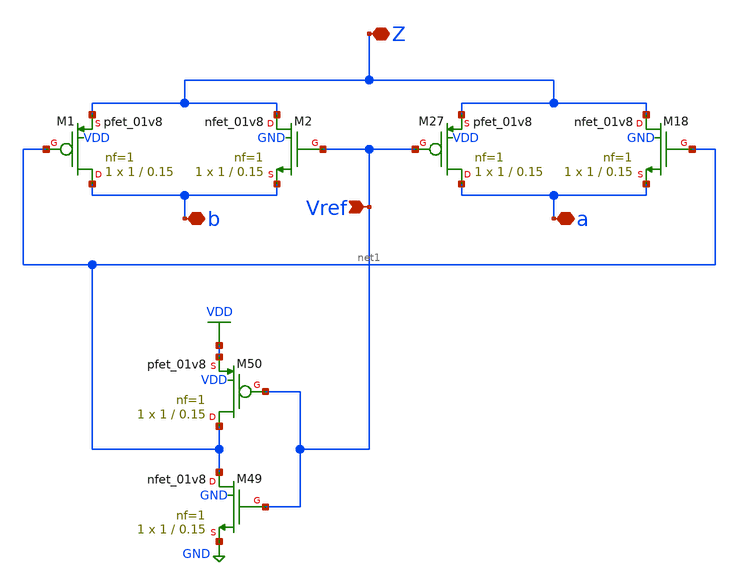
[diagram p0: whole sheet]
** sch_path: switch.sch
**.subckt switch Vref Z a b
*.ipin Vref
*.iopin Z
*.iopin a
*.iopin b
XM27 a Vref Z VDD sky130_fd_pr__pfet_01v8 L=0.15 W=1 nf=1 ad='int((1 + 1)/2) * 1 / 1 * 0.29' as='int((1 + 2)/2) * 1 / 1 * 0.29'
+ pd='2*int((1 + 1)/2) * (1 / 1 + 0.29)' ps='2*int((1 + 2)/2) * (1 / 1 + 0.29)' nrd='0.29 / 1 ' nrs='0.29 / 1 '
+ sa=0 sb=0 sd=0 mult=1 m=1
XM18 Z net1 a GND sky130_fd_pr__nfet_01v8 L=0.15 W=1 nf=1 ad='int((nf+1)/2) * W/nf * 0.29' as='int((nf+2)/2) * W/nf * 0.29'
+ pd='2*int((nf+1)/2) * (W/nf + 0.29)' ps='2*int((nf+2)/2) * (W/nf + 0.29)' nrd='0.29 / W' nrs='0.29 / W'
+ sa=0 sb=0 sd=0 mult=1 m=1
XM1 b net1 Z VDD sky130_fd_pr__pfet_01v8 L=0.15 W=1 nf=1 ad='int((1 + 1)/2) * 1 / 1 * 0.29' as='int((1 + 2)/2) * 1 / 1 * 0.29'
+ pd='2*int((1 + 1)/2) * (1 / 1 + 0.29)' ps='2*int((1 + 2)/2) * (1 / 1 + 0.29)' nrd='0.29 / 1 ' nrs='0.29 / 1 '
+ sa=0 sb=0 sd=0 mult=1 m=1
XM2 Z Vref b GND sky130_fd_pr__nfet_01v8 L=0.15 W=1 nf=1 ad='int((nf+1)/2) * W/nf * 0.29' as='int((nf+2)/2) * W/nf * 0.29'
+ pd='2*int((nf+1)/2) * (W/nf + 0.29)' ps='2*int((nf+2)/2) * (W/nf + 0.29)' nrd='0.29 / W' nrs='0.29 / W'
+ sa=0 sb=0 sd=0 mult=1 m=1
XM49 net1 Vref GND GND sky130_fd_pr__nfet_01v8 L=0.15 W=1 nf=1 ad='int((nf+1)/2) * W/nf * 0.29' as='int((nf+2)/2) * W/nf * 0.29'
+ pd='2*int((nf+1)/2) * (W/nf + 0.29)' ps='2*int((nf+2)/2) * (W/nf + 0.29)' nrd='0.29 / W' nrs='0.29 / W'
+ sa=0 sb=0 sd=0 mult=1 m=1
XM50 net1 Vref VDD VDD sky130_fd_pr__pfet_01v8 L=0.15 W=1 nf=1 ad='int((1 + 1)/2) * 1 / 1 * 0.29' as='int((1 + 2)/2) * 1 / 1 * 0.29'
+ pd='2*int((1 + 1)/2) * (1 / 1 + 0.29)' ps='2*int((1 + 2)/2) * (1 / 1 + 0.29)' nrd='0.29 / 1 ' nrs='0.29 / 1 '
+ sa=0 sb=0 sd=0 mult=1 m=1
**.ends
.GLOBAL GND
.GLOBAL VDD
.end
